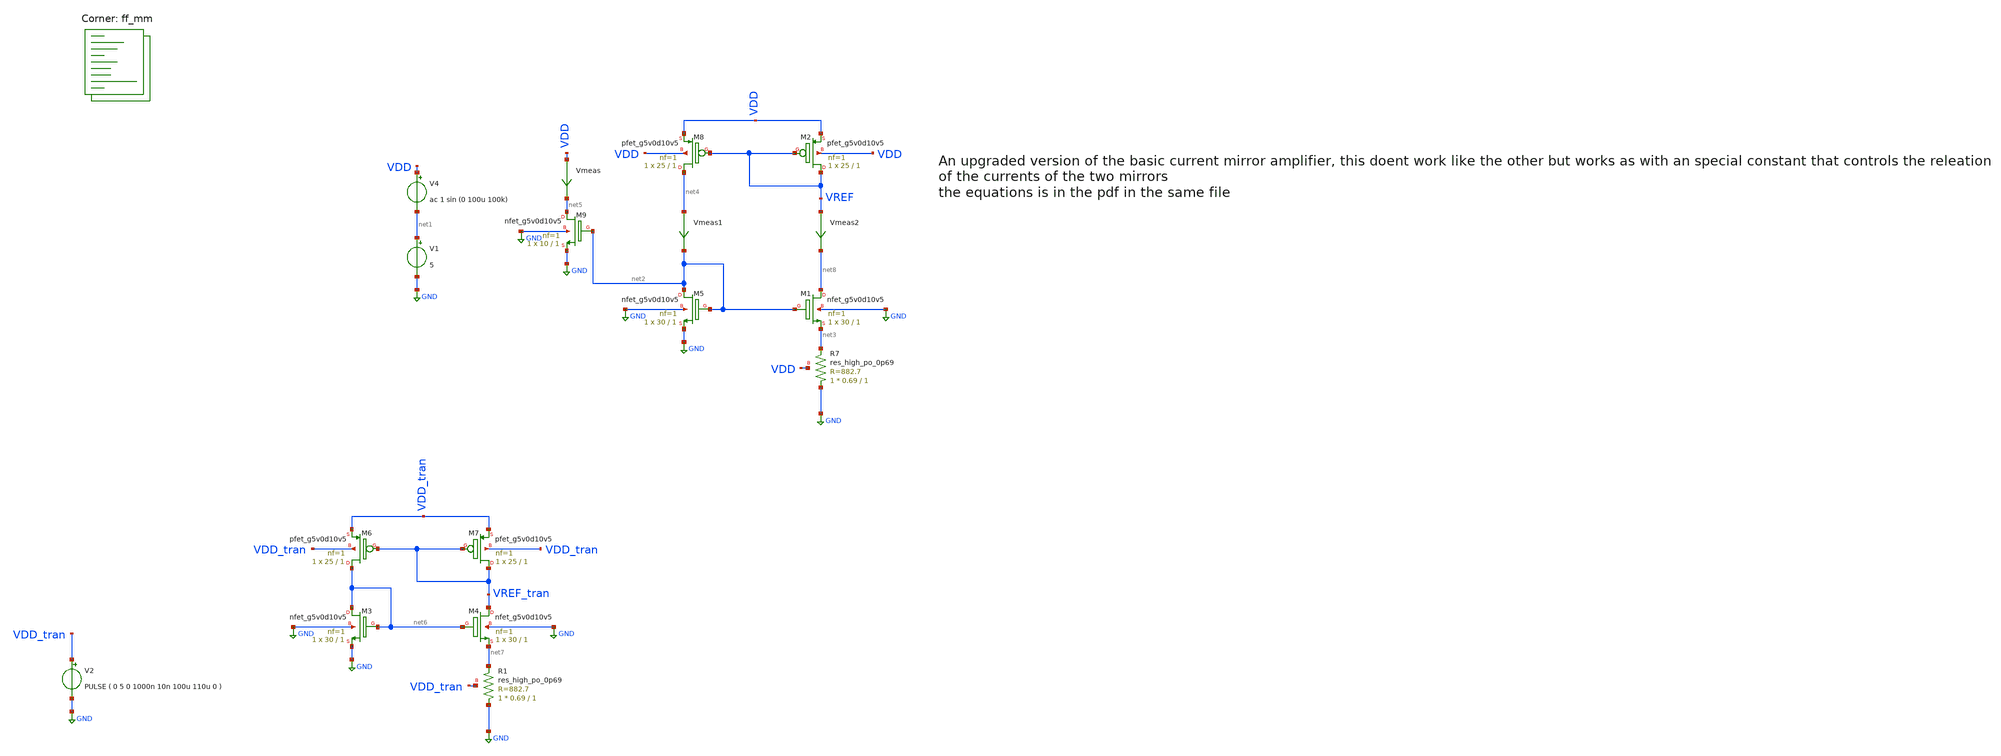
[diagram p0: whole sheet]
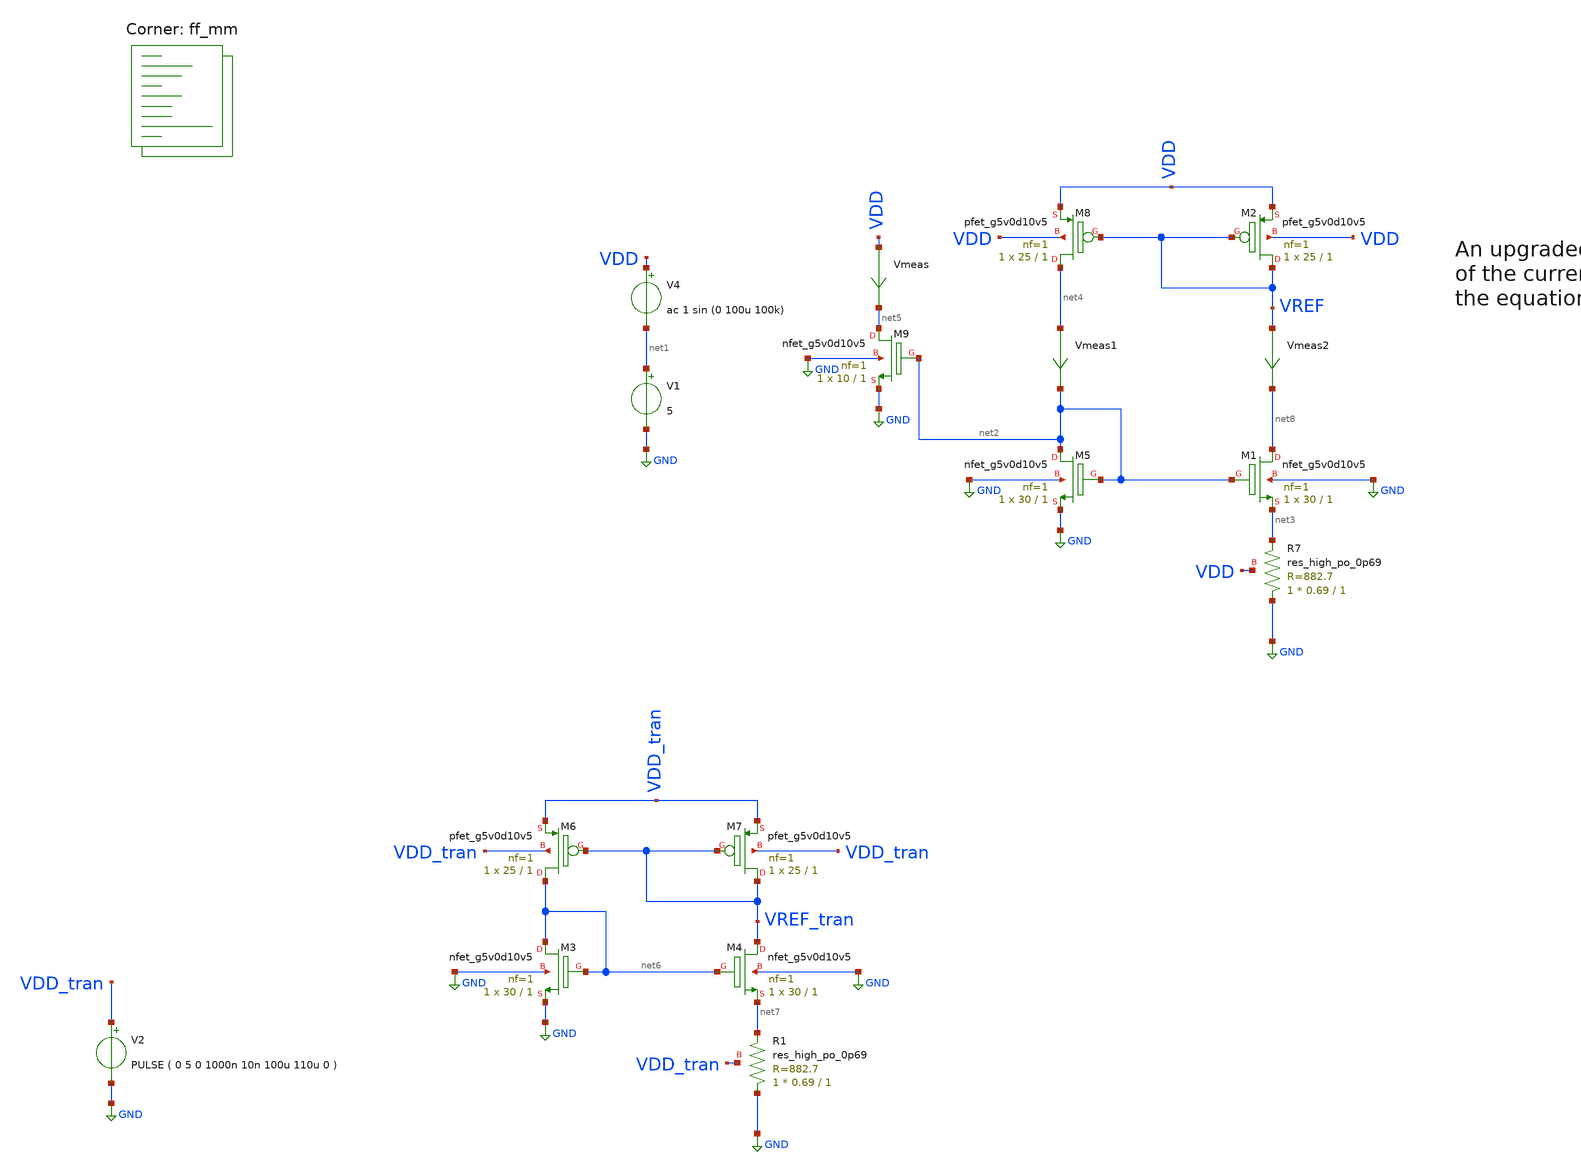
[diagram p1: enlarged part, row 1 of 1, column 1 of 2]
** sch_path: bandgaps/nmos_bandgap_with_resistance/bandgap.sch
**.subckt bandgap
V1 net1 GND 5
V2 VDD_tran GND PULSE ( 0 5 0 1000n 10n 100u 110u 0 )
XM5 net2 net2 GND GND sky130_fd_pr__nfet_g5v0d10v5 L=1 W=30 nf=1 ad='int((1 + 1)/2) * 30 / 1 * 0.29'
+ as='int((1 + 2)/2) * 30 / 1 * 0.29' pd='2*int((1 + 1)/2) * (30 / 1 + 0.29)' ps='2*int((1 + 2)/2) * (30 / 1 + 0.29)'
+ nrd='0.29 / 30 ' nrs='0.29 / 30 ' sa=0 sb=0 sd=0 mult=1 m=1
XM1 net8 net2 net3 GND sky130_fd_pr__nfet_g5v0d10v5 L=1 W=30 nf=1 ad='int((1 + 1)/2) * 30 / 1 * 0.29'
+ as='int((1 + 2)/2) * 30 / 1 * 0.29' pd='2*int((1 + 1)/2) * (30 / 1 + 0.29)' ps='2*int((1 + 2)/2) * (30 / 1 + 0.29)'
+ nrd='0.29 / 30 ' nrs='0.29 / 30 ' sa=0 sb=0 sd=0 mult=1 m=1
XM2 VREF VREF VDD VDD sky130_fd_pr__pfet_g5v0d10v5 L=1 W=25 nf=1 ad='int((1 + 1)/2) * 25 / 1 * 0.29'
+ as='int((1 + 2)/2) * 25 / 1 * 0.29' pd='2*int((1 + 1)/2) * (25 / 1 + 0.29)' ps='2*int((1 + 2)/2) * (25 / 1 + 0.29)'
+ nrd='0.29 / 25 ' nrs='0.29 / 25 ' sa=0 sb=0 sd=0 mult=1 m=1
XM8 net4 VREF VDD VDD sky130_fd_pr__pfet_g5v0d10v5 L=1 W=25 nf=1 ad='int((1 + 1)/2) * 25 / 1 * 0.29'
+ as='int((1 + 2)/2) * 25 / 1 * 0.29' pd='2*int((1 + 1)/2) * (25 / 1 + 0.29)' ps='2*int((1 + 2)/2) * (25 / 1 + 0.29)'
+ nrd='0.29 / 25 ' nrs='0.29 / 25 ' sa=0 sb=0 sd=0 mult=1 m=1
V4 VDD net1 ac 1 sin (0 100u 100k)
XM9 net5 net2 GND GND sky130_fd_pr__nfet_g5v0d10v5 L=1 W=10 nf=1 ad='int((1 + 1)/2) * 10 / 1 * 0.29'
+ as='int((1 + 2)/2) * 10 / 1 * 0.29' pd='2*int((1 + 1)/2) * (10 / 1 + 0.29)' ps='2*int((1 + 2)/2) * (10 / 1 + 0.29)'
+ nrd='0.29 / 10 ' nrs='0.29 / 10 ' sa=0 sb=0 sd=0 mult=1 m=1
Vmeas VDD net5 0
.save i(vmeas)
XM3 net6 net6 GND GND sky130_fd_pr__nfet_g5v0d10v5 L=1 W=30 nf=1 ad='int((1 + 1)/2) * 30 / 1 * 0.29'
+ as='int((1 + 2)/2) * 30 / 1 * 0.29' pd='2*int((1 + 1)/2) * (30 / 1 + 0.29)' ps='2*int((1 + 2)/2) * (30 / 1 + 0.29)'
+ nrd='0.29 / 30 ' nrs='0.29 / 30 ' sa=0 sb=0 sd=0 mult=1 m=1
XM4 VREF_tran net6 net7 GND sky130_fd_pr__nfet_g5v0d10v5 L=1 W=30 nf=1 ad='int((1 + 1)/2) * 30 / 1 * 0.29'
+ as='int((1 + 2)/2) * 30 / 1 * 0.29' pd='2*int((1 + 1)/2) * (30 / 1 + 0.29)' ps='2*int((1 + 2)/2) * (30 / 1 + 0.29)'
+ nrd='0.29 / 30 ' nrs='0.29 / 30 ' sa=0 sb=0 sd=0 mult=1 m=1
Vmeas1 net4 net2 0
.save i(vmeas1)
Vmeas2 VREF net8 0
.save i(vmeas2)
XR7 GND net3 VDD sky130_fd_pr__res_high_po_0p69 L=1 mult=1 m=1
XM6 net6 VREF_tran VDD_tran VDD_tran sky130_fd_pr__pfet_g5v0d10v5 L=1 W=25 nf=1 ad='int((1 + 1)/2) * 25 / 1 * 0.29'
+ as='int((1 + 2)/2) * 25 / 1 * 0.29' pd='2*int((1 + 1)/2) * (25 / 1 + 0.29)' ps='2*int((1 + 2)/2) * (25 / 1 + 0.29)'
+ nrd='0.29 / 25 ' nrs='0.29 / 25 ' sa=0 sb=0 sd=0 mult=1 m=1
XM7 VREF_tran VREF_tran VDD_tran VDD_tran sky130_fd_pr__pfet_g5v0d10v5 L=1 W=25 nf=1 ad='int((1 + 1)/2) * 25 / 1 * 0.29'
+ as='int((1 + 2)/2) * 25 / 1 * 0.29' pd='2*int((1 + 1)/2) * (25 / 1 + 0.29)' ps='2*int((1 + 2)/2) * (25 / 1 + 0.29)'
+ nrd='0.29 / 25 ' nrs='0.29 / 25 ' sa=0 sb=0 sd=0 mult=1 m=1
XR1 GND net7 VDD_tran sky130_fd_pr__res_high_po_0p69 L=1 mult=1 m=1
**** begin user architecture code

**************************************************************
**************************************************************
**************************************************************
**************************************************************
**************************************************************
*LIBs*********************************************************
**************************************************************
**************************************************************
**************************************************************
**************************************************************
**************************************************************
*.lib $::SKYWATER_MODELS/sky130.lib.spice tt
* chose the corners in the corner file
* tt_mm for mismatch
* ss ff sf fs standart corners
* ll hh lh hl capacitor and resistors corners
* mc for total process variation including corners
**************************************************************
**************************************************************
**************************************************************
**************************************************************
**************************************************************
*Corners/montecarlo options***********************************
**************************************************************
**************************************************************
**************************************************************
**************************************************************
**************************************************************
.TEMP 27
**************************************************************
**************************************************************
**************************************************************
**************************************************************
*SIMULATION and Plots*****************************************
**************************************************************
**************************************************************
**************************************************************
**************************************************************
.control
save all
dc TEMP -20 140 0.01
plot v(VREF)
plot i(VMEAS)
tran 10ns 10us
plot v(VREF_tran)
plot i(VMEAS1)  i(VMEAS2)
ac dec 20 1 1000G
plot db(v(VREF))

.endc

.lib $::SKYWATER_MODELS/sky130.lib.spice ff_mm
**** end user architecture code
**.ends
.GLOBAL GND
.end
